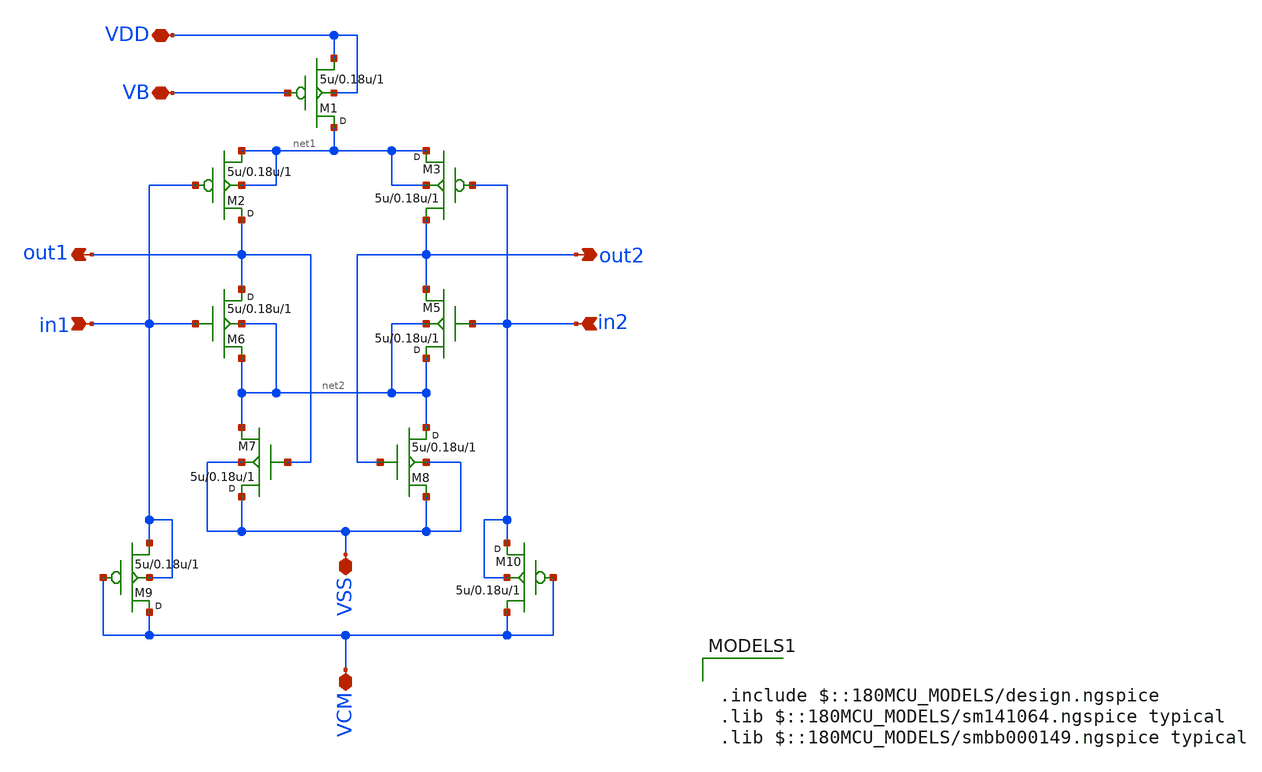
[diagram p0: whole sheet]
** sch_path: Schematics & Results/FULL_SCH_FILE/INA/INA_STAGE_FIXED.sch
**.subckt INA_STAGE_FIXED out1 out2 in1 in2 VDD VB VSS VCM
*.opin out1
*.opin out2
*.ipin in1
*.ipin in2
*.iopin VDD
*.iopin VB
*.iopin VSS
*.iopin VCM
M1 net1 VB VDD VDD pmos w=5u l=0.18u m=1
M2 out1 in1 net1 net1 pmos w=5u l=0.18u m=1
M3 net1 in2 out2 net1 pmos w=5u l=0.18u m=1
M5 net2 in2 out2 net2 nmos w=5u l=0.18u m=1
M6 out1 in1 net2 net2 nmos w=5u l=0.18u m=1
M7 VSS out1 net2 VSS nmos w=5u l=0.18u m=1
M8 net2 out2 VSS VSS nmos w=5u l=0.18u m=1
M9 VCM VCM in1 in1 pmos w=5u l=0.18u m=1
M10 in2 VCM VCM in2 pmos w=5u l=0.18u m=1
**** begin user architecture code

.include $::180MCU_MODELS/design.ngspice
.lib $::180MCU_MODELS/sm141064.ngspice typical
.lib $::180MCU_MODELS/smbb000149.ngspice typical

**** end user architecture code
**.ends
.end
